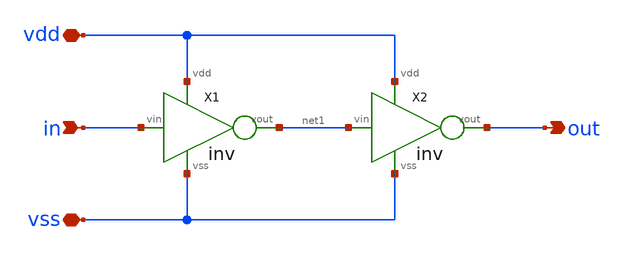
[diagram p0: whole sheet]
** sch_path: xsch/ip/logic/buffer/buffer.sch
**.subckt buffer in out vdd vss
*.ipin in
*.opin out
*.iopin vdd
*.iopin vss
X1 in net1 vdd vss inv
X2 net1 out vdd vss inv
**.ends

* expanding   symbol:  /home/bmott/ttsky25b_tiny_chaos/xsch/ip/logic/inv/inv.sym # of pins=4
** sym_path: xsch/ip/logic/inv/inv.sym
** sch_path: xsch/ip/logic/inv/inv.sch
.subckt inv vin vout vdd vss
*.ipin vin
*.opin vout
*.ipin vdd
*.ipin vss
XMn vout vin vss vss sky130_fd_pr__nfet_01v8 L=0.15 W=1 nf=1 ad='int((1 + 1)/2) * 1 / 1 * 0.29' as='int((1 + 2)/2) * 1 / 1 * 0.29'
+ pd='2*int((1 + 1)/2) * (1 / 1 + 0.29)' ps='2*int((1 + 2)/2) * (1 / 1 + 0.29)' nrd='0.29 / 1 ' nrs='0.29 / 1 '
+ sa=0 sb=0 sd=0 mult=1 m=1
XMp vout vin vdd vdd sky130_fd_pr__pfet_01v8 L=0.15 W=2 nf=1 ad='int((nf+1)/2) * W/nf * 0.29' as='int((nf+2)/2) * W/nf * 0.29'
+ pd='2*int((nf+1)/2) * (W/nf + 0.29)' ps='2*int((nf+2)/2) * (W/nf + 0.29)' nrd='0.29 / W' nrs='0.29 / W'
+ sa=0 sb=0 sd=0 mult=1 m=1
.ends

.end
